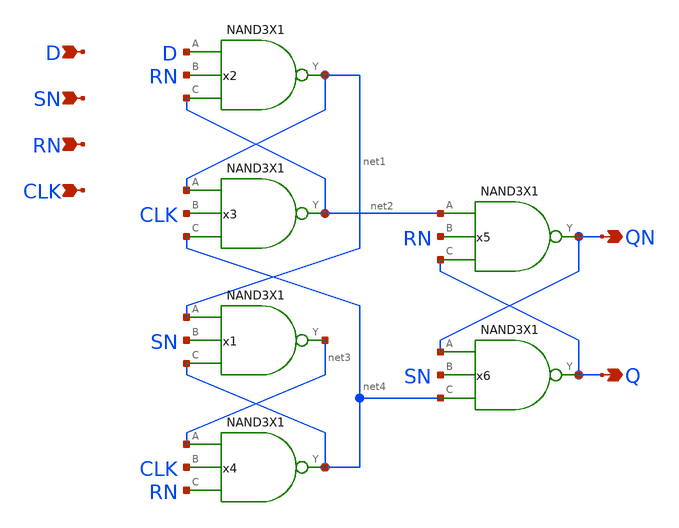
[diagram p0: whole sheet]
** sch_path: lib/xschem/DFFSNRNX1.sch
**.subckt DFFSNRNX1 D QN SN CLK Q RN
*.ipin D
*.opin QN
*.ipin SN
*.ipin CLK
*.opin Q
*.ipin RN
x1 net3 net1 SN net4 VDD VSS NAND3X1
x3 net2 net1 CLK net4 VDD VSS NAND3X1
x6 Q QN SN net4 VDD VSS NAND3X1
x2 net1 D RN net2 VDD VSS NAND3X1
x4 net4 net3 CLK RN VDD VSS NAND3X1
x5 QN net2 RN Q VDD VSS NAND3X1
**.ends

* expanding   symbol:  NAND3X1.sym # of pins=4
** sym_path: lib/xschem/NAND3X1.sym
** sch_path: lib/xschem/NAND3X1.sch
.subckt NAND3X1 Y A B C VDD VSS
*.ipin A
*.opin Y
*.ipin B
*.ipin C
XM1 net2 C VSS VSS sky130_fd_pr__nfet_01v8 L=0.15 W=3 nf=1 ad='int((nf+1)/2) * W/nf * 0.29' as='int((nf+2)/2) * W/nf * 0.29'
+ pd='2*int((nf+1)/2) * (W/nf + 0.29)' ps='2*int((nf+2)/2) * (W/nf + 0.29)' nrd='0.29 / W' nrs='0.29 / W'
+ sa=0 sb=0 sd=0 mult=1 m=1
XM2 Y A VDD VDD sky130_fd_pr__pfet_01v8 L=0.15 W=2 nf=1 ad='int((nf+1)/2) * W/nf * 0.29' as='int((nf+2)/2) * W/nf * 0.29'
+ pd='2*int((nf+1)/2) * (W/nf + 0.29)' ps='2*int((nf+2)/2) * (W/nf + 0.29)' nrd='0.29 / W' nrs='0.29 / W'
+ sa=0 sb=0 sd=0 mult=1 m=1
XM3 net1 B net2 VSS sky130_fd_pr__nfet_01v8 L=0.15 W=3 nf=1 ad='int((nf+1)/2) * W/nf * 0.29' as='int((nf+2)/2) * W/nf * 0.29'
+ pd='2*int((nf+1)/2) * (W/nf + 0.29)' ps='2*int((nf+2)/2) * (W/nf + 0.29)' nrd='0.29 / W' nrs='0.29 / W'
+ sa=0 sb=0 sd=0 mult=1 m=1
XM4 Y A net1 VSS sky130_fd_pr__nfet_01v8 L=0.15 W=3 nf=1 ad='int((nf+1)/2) * W/nf * 0.29' as='int((nf+2)/2) * W/nf * 0.29'
+ pd='2*int((nf+1)/2) * (W/nf + 0.29)' ps='2*int((nf+2)/2) * (W/nf + 0.29)' nrd='0.29 / W' nrs='0.29 / W'
+ sa=0 sb=0 sd=0 mult=1 m=1
XM5 Y A VDD VDD sky130_fd_pr__pfet_01v8 L=0.15 W=2 nf=1 ad='int((nf+1)/2) * W/nf * 0.29' as='int((nf+2)/2) * W/nf * 0.29'
+ pd='2*int((nf+1)/2) * (W/nf + 0.29)' ps='2*int((nf+2)/2) * (W/nf + 0.29)' nrd='0.29 / W' nrs='0.29 / W'
+ sa=0 sb=0 sd=0 mult=1 m=1
XM6 Y B VDD VDD sky130_fd_pr__pfet_01v8 L=0.15 W=2 nf=1 ad='int((nf+1)/2) * W/nf * 0.29' as='int((nf+2)/2) * W/nf * 0.29'
+ pd='2*int((nf+1)/2) * (W/nf + 0.29)' ps='2*int((nf+2)/2) * (W/nf + 0.29)' nrd='0.29 / W' nrs='0.29 / W'
+ sa=0 sb=0 sd=0 mult=1 m=1
XM7 Y B VDD VDD sky130_fd_pr__pfet_01v8 L=0.15 W=2 nf=1 ad='int((nf+1)/2) * W/nf * 0.29' as='int((nf+2)/2) * W/nf * 0.29'
+ pd='2*int((nf+1)/2) * (W/nf + 0.29)' ps='2*int((nf+2)/2) * (W/nf + 0.29)' nrd='0.29 / W' nrs='0.29 / W'
+ sa=0 sb=0 sd=0 mult=1 m=1
XM8 Y C VDD VDD sky130_fd_pr__pfet_01v8 L=0.15 W=2 nf=1 ad='int((nf+1)/2) * W/nf * 0.29' as='int((nf+2)/2) * W/nf * 0.29'
+ pd='2*int((nf+1)/2) * (W/nf + 0.29)' ps='2*int((nf+2)/2) * (W/nf + 0.29)' nrd='0.29 / W' nrs='0.29 / W'
+ sa=0 sb=0 sd=0 mult=1 m=1
XM9 Y C VDD VDD sky130_fd_pr__pfet_01v8 L=0.15 W=2 nf=1 ad='int((nf+1)/2) * W/nf * 0.29' as='int((nf+2)/2) * W/nf * 0.29'
+ pd='2*int((nf+1)/2) * (W/nf + 0.29)' ps='2*int((nf+2)/2) * (W/nf + 0.29)' nrd='0.29 / W' nrs='0.29 / W'
+ sa=0 sb=0 sd=0 mult=1 m=1
.ends

.end
